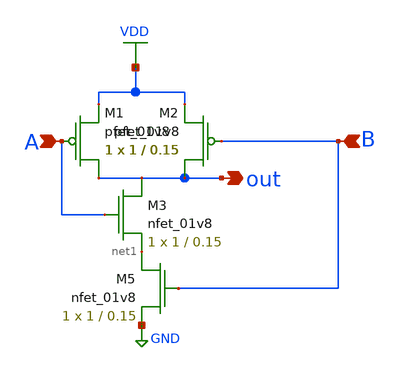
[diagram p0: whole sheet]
** sch_path: MP1/NAND_mp1.sch
**.subckt NAND_mp1 A B out
*.ipin A
*.ipin B
*.opin out
XM1 out A VDD VDD sky130_fd_pr__pfet_01v8 L=0.15 W=1 nf=1 ad='int((nf+1)/2) * W/nf * 0.29' as='int((nf+2)/2) * W/nf * 0.29'
+ pd='2*int((nf+1)/2) * (W/nf + 0.29)' ps='2*int((nf+2)/2) * (W/nf + 0.29)' nrd='0.29 / W' nrs='0.29 / W'
+ sa=0 sb=0 sd=0 mult=1 m=1
XM2 out B VDD VDD sky130_fd_pr__pfet_01v8 L=0.15 W=1 nf=1 ad='int((nf+1)/2) * W/nf * 0.29' as='int((nf+2)/2) * W/nf * 0.29'
+ pd='2*int((nf+1)/2) * (W/nf + 0.29)' ps='2*int((nf+2)/2) * (W/nf + 0.29)' nrd='0.29 / W' nrs='0.29 / W'
+ sa=0 sb=0 sd=0 mult=1 m=1
XM3 out A net1 GND sky130_fd_pr__nfet_01v8 L=0.15 W=1 nf=1 ad='int((nf+1)/2) * W/nf * 0.29' as='int((nf+2)/2) * W/nf * 0.29'
+ pd='2*int((nf+1)/2) * (W/nf + 0.29)' ps='2*int((nf+2)/2) * (W/nf + 0.29)' nrd='0.29 / W' nrs='0.29 / W'
+ sa=0 sb=0 sd=0 mult=1 m=1
XM5 net1 B GND GND sky130_fd_pr__nfet_01v8 L=0.15 W=1 nf=1 ad='int((nf+1)/2) * W/nf * 0.29' as='int((nf+2)/2) * W/nf * 0.29'
+ pd='2*int((nf+1)/2) * (W/nf + 0.29)' ps='2*int((nf+2)/2) * (W/nf + 0.29)' nrd='0.29 / W' nrs='0.29 / W'
+ sa=0 sb=0 sd=0 mult=1 m=1
**.ends
.GLOBAL VDD
.GLOBAL GND
.end
